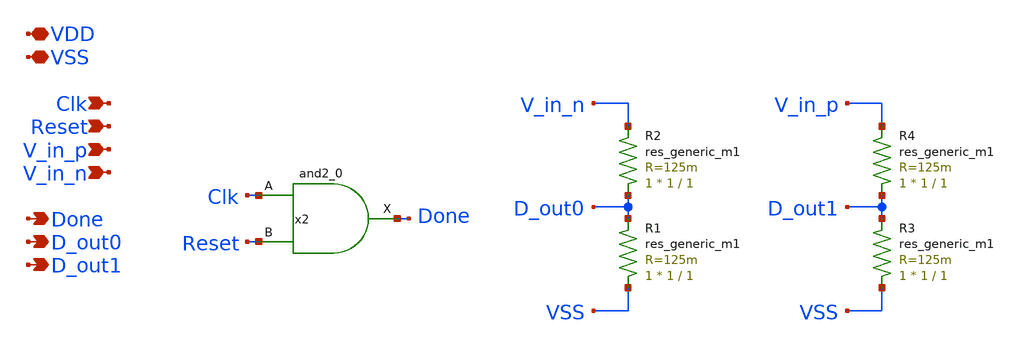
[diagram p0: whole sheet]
** sch_path: xschem/src/sar-adc/sar-adc.sch
**.subckt sar-adc VDD V_in_p Done VSS V_in_n Reset D_out0 D_out1 Clk
*.iopin VDD
*.ipin V_in_p
*.opin Done
*.iopin VSS
*.ipin V_in_n
*.ipin Reset
*.opin D_out0
*.opin D_out1
*.ipin Clk
R1 VSS D_out0 sky130_fd_pr__res_generic_m1 W=1 L=1 m=1
R2 D_out0 V_in_n sky130_fd_pr__res_generic_m1 W=1 L=1 m=1
R3 VSS D_out1 sky130_fd_pr__res_generic_m1 W=1 L=1 m=1
R4 D_out1 V_in_p sky130_fd_pr__res_generic_m1 W=1 L=1 m=1
x2 Clk Reset VSS VSS VDD VDD Done sky130_fd_sc_hd__and2_0
**** begin user architecture code
 .include $::SKYWATER_STDCELLS/sky130_fd_sc_hd.spice

**** end user architecture code
**.ends
.end
